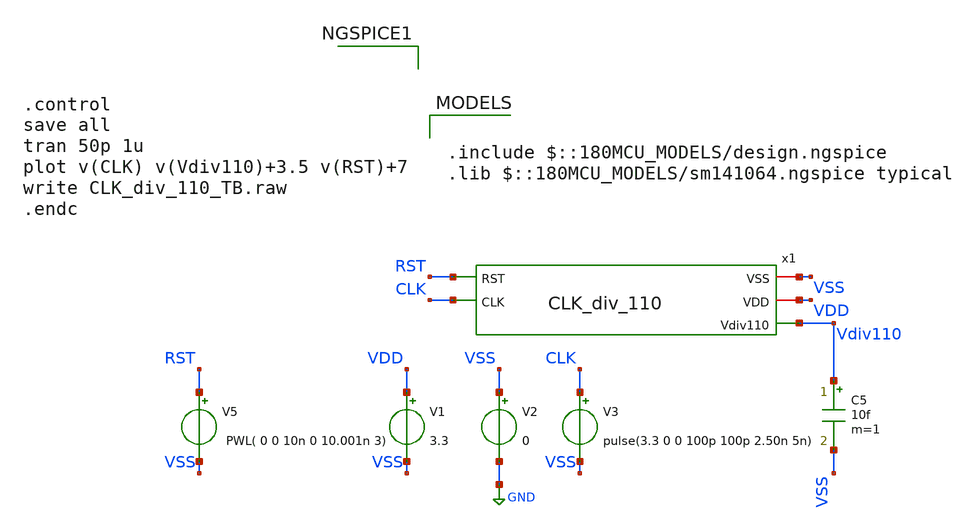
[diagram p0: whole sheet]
** sch_path: Clock_Generator_PAKISTAN_02/Schematics/CLK_div_110_TB.sch
**.subckt CLK_div_110_TB
V1 VDD VSS 3.3
V2 VSS GND 0
V3 CLK VSS pulse(3.3 0 0 100p 100p 2.50n 5n)
C5 Vdiv110 VSS 10f m=1
V5 RST VSS PWL( 0 0 10n 0 10.001n 3)
x1 VSS VDD RST Vdiv110 CLK CLK_div_110
**** begin user architecture code

.include $::180MCU_MODELS/design.ngspice
.lib $::180MCU_MODELS/sm141064.ngspice typical




.control
save all
tran 50p 1u
plot v(CLK) v(Vdiv110)+3.5 v(RST)+7
write CLK_div_110_TB.raw
.endc


**** end user architecture code
**.ends
.GLOBAL GND
.end
